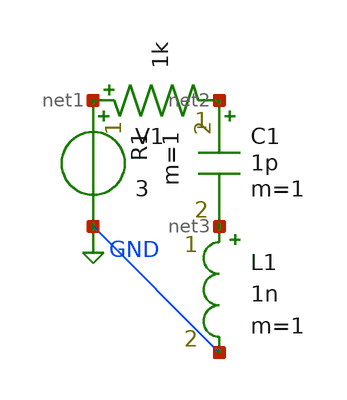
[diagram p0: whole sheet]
** sch_path: lib/Organize_into_Examples_or_pdk_examples/RLCCircuit.sch
**.subckt RLCCircuit
V1 net1 GND 3
R1 net1 net2 1k m=1
C1 net2 net3 1p m=1
L1 net3 GND 1n m=1
**** begin user architecture code



.lib

.control

.endc

.save all



**** end user architecture code
**.ends
.GLOBAL GND
.end
